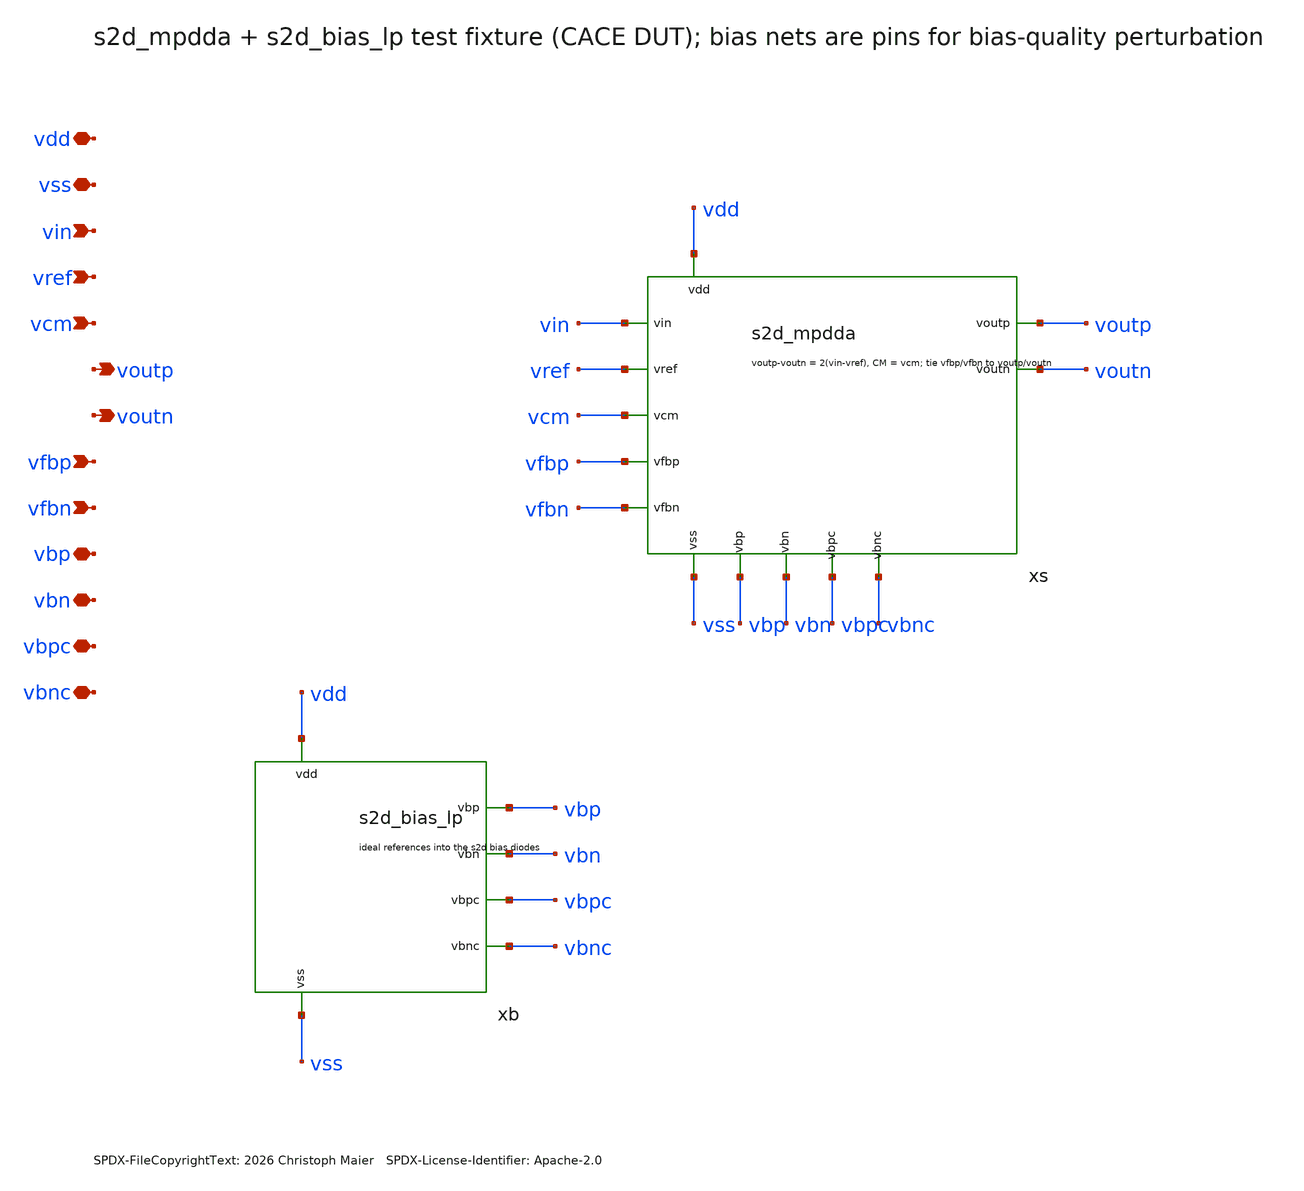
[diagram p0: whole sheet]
** sch_path: sudelbuecher/design_considerations/s2d_input_buffer/xschem/s2d_mpdda_biased.sch
* SPDX-FileCopyrightText: 2026 Christoph Maier SPDX-License-Identifier: Apache-2.0
**.subckt s2d_mpdda_biased vdd vss vin vref vcm voutp voutn vfbp vfbn vbp vbn vbpc vbnc
*.iopin vdd
*.iopin vss
*.ipin vin
*.ipin vref
*.ipin vcm
*.opin voutp
*.opin voutn
*.ipin vfbp
*.ipin vfbn
*.iopin vbp
*.iopin vbn
*.iopin vbpc
*.iopin vbnc
xs vdd vss vin vref vcm voutp voutn vfbp vfbn vbp vbn vbpc vbnc s2d_mpdda
xb vdd vss vbp vbn vbpc vbnc s2d_bias_lp
**.ends

* expanding   symbol:  s2d_mpdda.sym # of pins=13
** sym_path: macros/sg13cmos5l_IOPadSingle2Diff/schematic/xschem/s2d_mpdda.sym
** sch_path: macros/sg13cmos5l_IOPadSingle2Diff/schematic/xschem/s2d_mpdda.sch
.subckt s2d_mpdda vdd vss vin vref vcm voutp voutn vfbp vfbn vbp vbn vbpc vbnc
*.iopin vdd
*.iopin vss
*.ipin vin
*.ipin vref
*.ipin vcm
*.opin voutp
*.opin voutn
*.ipin vfbp
*.ipin vfbn
*.iopin vbp
*.iopin vbn
*.iopin vbpc
*.iopin vbnc
XA1 x y vin vref vdd vss vbp unit_r2
XA2 x y vin vref vdd vss vbp unit_r2
XF1 x y vcm vfbp vdd vss vbp unit_r2
XF2 x y vfbn vcm vdd vss vbp unit_r2
XLP lp vcmfb vdd vdd sg13_hv_pmos w=24u l=4u ng=4 m=1 mm_ok=1
XLPC voutp vbpc lp vdd sg13_hv_pmos w=30u l=3u ng=2 m=1 mm_ok=1
XCX voutp vbnc x vss sg13_hv_nmos w=30u l=3u ng=2 m=1 mm_ok=1
XSX x vbn vss vss sg13_hv_nmos w=36u l=6u ng=6 m=1 mm_ok=1
XLN ln vcmfb vdd vdd sg13_hv_pmos w=24u l=4u ng=4 m=1 mm_ok=1
XLNC voutn vbpc ln vdd sg13_hv_pmos w=30u l=3u ng=2 m=1 mm_ok=1
XCY voutn vbnc y vss sg13_hv_nmos w=30u l=3u ng=2 m=1 mm_ok=1
XSY y vbn vss vss sg13_hv_nmos w=36u l=6u ng=6 m=1 mm_ok=1
XCLP vss voutp vss vss sg13_hv_nmos w=12u l=12u ng=1 m=1 mm_ok=1
XCLN vss voutn vss vss sg13_hv_nmos w=12u l=12u ng=1 m=1 mm_ok=1
XM1 xc yc vfbp vcm vdd vss vbp unit_r2
XM2 xc yc vfbn vcm vdd vss vbp unit_r2
XD dd vcmfb vdd vdd sg13_hv_pmos w=24u l=4u ng=4 m=1 mm_ok=1
XDC vcmfb vbpc dd vdd sg13_hv_pmos w=30u l=3u ng=2 m=1 mm_ok=1
XCXC vcmfb vbnc xc vss sg13_hv_nmos w=30u l=3u ng=2 m=1 mm_ok=1
XSXC xc vbn vss vss sg13_hv_nmos w=24u l=6u ng=4 m=1 mm_ok=1
XCYC vdd vbnc yc vss sg13_hv_nmos w=30u l=3u ng=2 m=1 mm_ok=1
XSYC yc vbn vss vss sg13_hv_nmos w=24u l=6u ng=4 m=1 mm_ok=1
XMDL[3] vdd vcmfb vdd vdd sg13_hv_pmos w=1u l=4u ng=1 m=1 mm_ok=1
XMDL[2] vdd vcmfb vdd vdd sg13_hv_pmos w=1u l=4u ng=1 m=1 mm_ok=1
XMDL[1] vdd vcmfb vdd vdd sg13_hv_pmos w=1u l=4u ng=1 m=1 mm_ok=1
XMDL[0] vdd vcmfb vdd vdd sg13_hv_pmos w=1u l=4u ng=1 m=1 mm_ok=1
.ends


* expanding   symbol:  s2d_bias_lp.sym # of pins=6
** sym_path: sudelbuecher/design_considerations/s2d_input_buffer/xschem/s2d_bias_lp.sym
** sch_path: sudelbuecher/design_considerations/s2d_input_buffer/xschem/s2d_bias_lp.sch
.subckt s2d_bias_lp vdd vss vbp vbn vbpc vbnc
*.iopin vdd
*.iopin vss
*.iopin vbp
*.iopin vbn
*.iopin vbpc
*.iopin vbnc
XBP vbp vbp vdd vdd sg13_hv_pmos w=5u l=6u ng=1 m=1 mm_ok=1
IBP vbp vss 5u
XBPC vbpc vbpc vdd vdd sg13_hv_pmos w=1u l=4u ng=1 m=1 mm_ok=1
IBPC vbpc vss 2u
IBN vdd vbn 5u
XBN vbn vbn vss vss sg13_hv_nmos w=6u l=6u ng=1 m=1 mm_ok=1
IBNC vdd vbnc 2u
XBNC vbnc vbnc vss vss sg13_hv_nmos w=1u l=8u ng=1 m=1 mm_ok=1
.ends


* expanding   symbol:  unit_r2.sym # of pins=7
** sym_path: sudelbuecher/design_considerations/class_ab_pad_driver/improvements/xschem/unit_r2.sym
** sch_path: sudelbuecher/design_considerations/class_ab_pad_driver/improvements/xschem/unit_r2.sch
.subckt unit_r2 x y gp gn vdd vss vbp
*.opin x
*.opin y
*.ipin gp
*.ipin gn
*.iopin vdd
*.iopin vss
*.ipin vbp
XTa sa vbp vdd vdd sg13_hv_pmos w=5u l=6u ng=1 m=1 mm_ok=1
XTb sb vbp vdd vdd sg13_hv_pmos w=5u l=6u ng=1 m=1 mm_ok=1
XMa y gp sa sa sg13_hv_pmos w=20u l=1u ng=2 m=1 mm_ok=1
XMb x gn sb sb sg13_hv_pmos w=20u l=1u ng=2 m=1 mm_ok=1
XR sa sb vss rhigh w=0.5u l=50.6u m=1 b=0 mm_ok=1
.ends

.end
